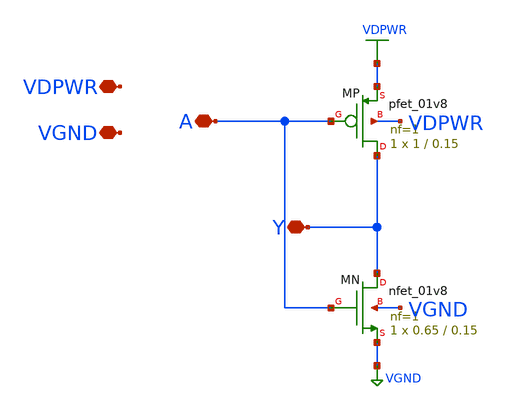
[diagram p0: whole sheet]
** sch_path: cells/ELAD1_INV/schematic/ELAD1_INV.sch
**.subckt ELAD1_INV A Y VDPWR VGND
*.iopin A
*.iopin Y
*.iopin VDPWR
*.iopin VGND
XMN Y A VGND VGND sky130_fd_pr__nfet_01v8 L=0.15 W=0.65 nf=1 ad='int((1 + 1)/2) * 0.65 / 1 * 0.29' as='int((1 + 2)/2) * 0.65 / 1 * 0.29'
+ pd='2*int((1 + 1)/2) * (0.65 / 1 + 0.29)' ps='2*int((1 + 2)/2) * (0.65 / 1 + 0.29)' nrd='0.29 / 0.65 '
+ nrs='0.29 / 0.65 ' sa=0 sb=0 sd=0 mult=1 m=1
XMP Y A VDPWR VDPWR sky130_fd_pr__pfet_01v8 L=0.15 W=1 nf=1 ad='int((nf+1)/2) * W/nf * 0.29' as='int((nf+2)/2) * W/nf * 0.29'
+ pd='2*int((nf+1)/2) * (W/nf + 0.29)' ps='2*int((nf+2)/2) * (W/nf + 0.29)' nrd='0.29 / W' nrs='0.29 / W'
+ sa=0 sb=0 sd=0 mult=1 m=1
**.ends
.GLOBAL VGND
.GLOBAL VDPWR
.end
